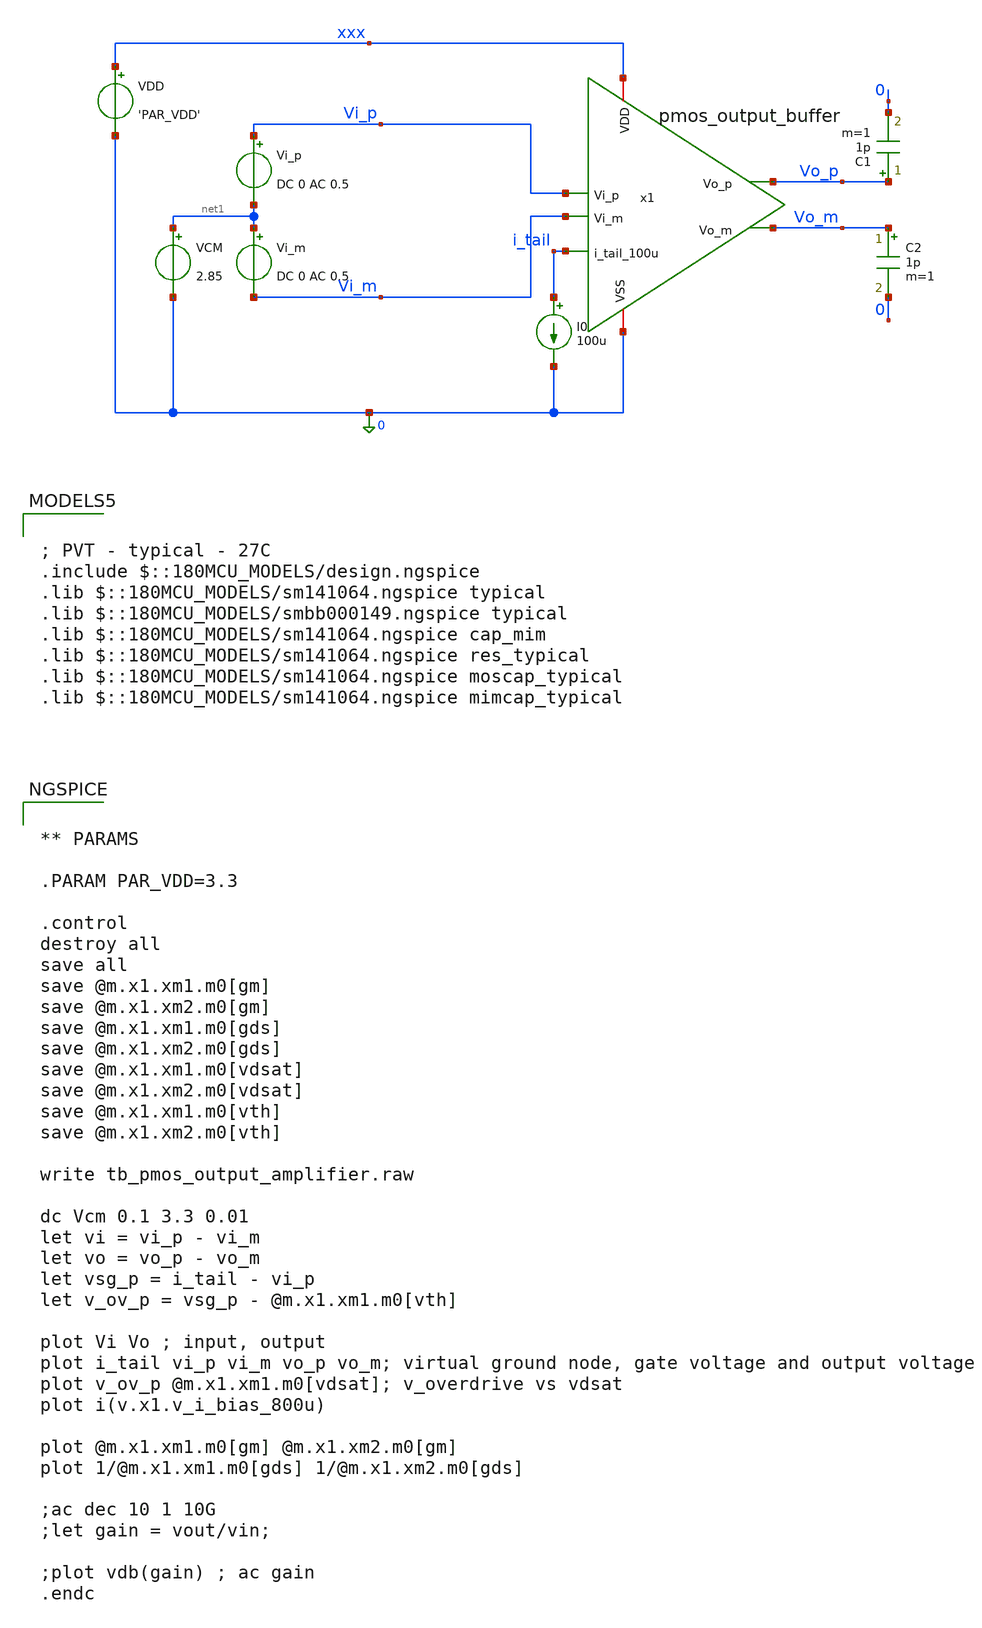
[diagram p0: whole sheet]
** sch_path: designs/output_amplifier/testbench/tb_pmos_output_amplifier.sch
**.subckt tb_pmos_output_amplifier
x1 xxx Vi_p 0 Vi_m Vo_p Vo_m i_tail pmos_output_buffer
VDD xxx 0 'PAR_VDD'
VCM net1 0 2.85
Vi_p Vi_p net1 DC 0 AC 0.5
Vi_m net1 Vi_m DC 0 AC 0.5
C1 Vo_p 0 1p m=1
C2 Vo_m 0 1p m=1
I0 i_tail 0 100u
**** begin user architecture code

; PVT - typical - 27C
.include $::180MCU_MODELS/design.ngspice
.lib $::180MCU_MODELS/sm141064.ngspice typical
.lib $::180MCU_MODELS/smbb000149.ngspice typical
.lib $::180MCU_MODELS/sm141064.ngspice cap_mim
.lib $::180MCU_MODELS/sm141064.ngspice res_typical
.lib $::180MCU_MODELS/sm141064.ngspice moscap_typical
.lib $::180MCU_MODELS/sm141064.ngspice mimcap_typical



** PARAMS

.PARAM PAR_VDD=3.3

.control
destroy all
save all
save @m.x1.xm1.m0[gm]
save @m.x1.xm2.m0[gm]
save @m.x1.xm1.m0[gds]
save @m.x1.xm2.m0[gds]
save @m.x1.xm1.m0[vdsat]
save @m.x1.xm2.m0[vdsat]
save @m.x1.xm1.m0[vth]
save @m.x1.xm2.m0[vth]

write tb_pmos_output_amplifier.raw

dc Vcm 0.1 3.3 0.01
let vi = vi_p - vi_m
let vo = vo_p - vo_m
let vsg_p = i_tail - vi_p
let v_ov_p = vsg_p - @m.x1.xm1.m0[vth]

plot Vi Vo ; input, output
plot i_tail vi_p vi_m vo_p vo_m; virtual ground node, gate voltage and output voltage
plot v_ov_p @m.x1.xm1.m0[vdsat]; v_overdrive vs vdsat
plot i(v.x1.v_i_bias_800u)

plot @m.x1.xm1.m0[gm] @m.x1.xm2.m0[gm]
plot 1/@m.x1.xm1.m0[gds] 1/@m.x1.xm2.m0[gds]

;ac dec 10 1 10G
;let gain = vout/vin;

;plot vdb(gain) ; ac gain
.endc


**** end user architecture code
**.ends

* expanding   symbol:  output_amplifier/schematic/pmos_output_buffer.sym # of pins=7
** sym_path: designs/output_amplifier/schematic/pmos_output_buffer.sym
** sch_path: designs/output_amplifier/schematic/pmos_output_buffer.sch
.subckt pmos_output_buffer VDD Vi_p VSS Vi_m Vo_p Vo_m i_tail_100u
*.iopin VDD
*.iopin VSS
*.ipin Vi_p
*.ipin Vi_m
*.opin Vo_p
*.opin Vo_m
*.ipin i_tail_100u
XM1 Vo_p Vi_p net1 VDD pfet_03v3 L=0.28u W=40u nf=10 ad='int((nf+1)/2) * W/nf * 0.18u' as='int((nf+2)/2) * W/nf * 0.18u'
+ pd='2*int((nf+1)/2) * (W/nf + 0.18u)' ps='2*int((nf+2)/2) * (W/nf + 0.18u)' nrd='0.18u / W' nrs='0.18u / W'
+ sa=0 sb=0 sd=0 m=1
XM2 Vo_m Vi_m net1 VDD pfet_03v3 L=0.28u W=40u nf=10 ad='int((nf+1)/2) * W/nf * 0.18u' as='int((nf+2)/2) * W/nf * 0.18u'
+ pd='2*int((nf+1)/2) * (W/nf + 0.18u)' ps='2*int((nf+2)/2) * (W/nf + 0.18u)' nrd='0.18u / W' nrs='0.18u / W'
+ sa=0 sb=0 sd=0 m=1
R1 Vo_m VSS 2k m=1
R2 Vo_p VSS 2k m=1
XM3 net2 i_tail_100u VDD VDD pfet_03v3 L=0.5u W=40u nf=10 ad='int((nf+1)/2) * W/nf * 0.18u' as='int((nf+2)/2) * W/nf * 0.18u'
+ pd='2*int((nf+1)/2) * (W/nf + 0.18u)' ps='2*int((nf+2)/2) * (W/nf + 0.18u)' nrd='0.18u / W' nrs='0.18u / W'
+ sa=0 sb=0 sd=0 m=1
XM4 i_tail_100u i_tail_100u VDD VDD pfet_03v3 L=0.5u W=4u nf=10 ad='int((nf+1)/2) * W/nf * 0.18u' as='int((nf+2)/2) * W/nf * 0.18u'
+ pd='2*int((nf+1)/2) * (W/nf + 0.18u)' ps='2*int((nf+2)/2) * (W/nf + 0.18u)' nrd='0.18u / W' nrs='0.18u / W'
+ sa=0 sb=0 sd=0 m=1
V_i_bias_800u net2 net1 0
.save i(v_i_bias_800u)
.ends

.end
